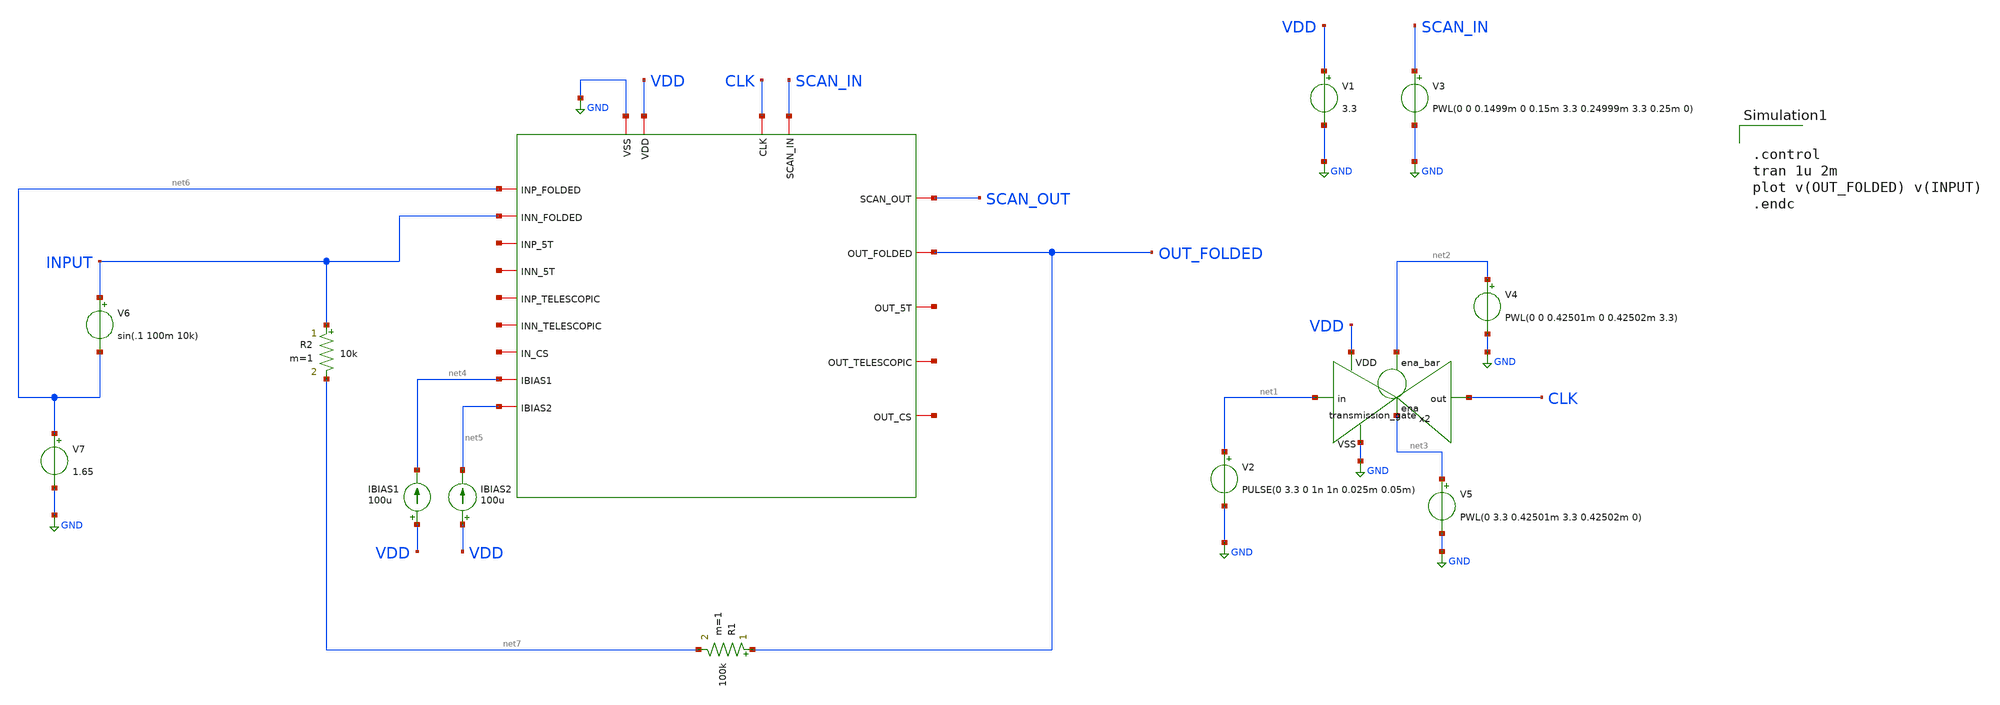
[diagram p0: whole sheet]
** sch_path: designs/libs/core_tb/system_tb.sch
**.subckt system_tb
x1 CLK SCAN_OUT SCAN_IN GND VDD OUT_FOLDED net6 net8 net5 net4 INPUT net9 net10 net11 net12 net13
+ net14 net15 DUT
V3 SCAN_IN GND PWL(0 0 0.1499m 0 0.15m 3.3 0.24999m 3.3 0.25m 0)
V1 VDD GND 3.3
V2 net1 GND PULSE(0 3.3 0 1n 1n 0.025m 0.05m)
x2 net2 VDD CLK net1 GND net3 transmission_gate
V4 net2 GND PWL(0 0 0.42501m 0 0.42502m 3.3)
V5 net3 GND PWL(0 3.3 0.42501m 3.3 0.42502m 0)
IBIAS1 VDD net4 100u
IBIAS2 VDD net5 100u
R1 OUT_FOLDED net7 100k m=1
R2 INPUT net7 10k m=1
V6 INPUT net6 sin(.1 100m 10k)
V7 net6 GND 1.65
**** begin user architecture code

.include $::180MCU_MODELS/design.ngspice
.lib $::180MCU_MODELS/sm141064.ngspice typical



.control
tran 1u 2m
plot v(OUT_FOLDED) v(INPUT)
.endc


**** end user architecture code
**.ends
.GLOBAL GND
.end
